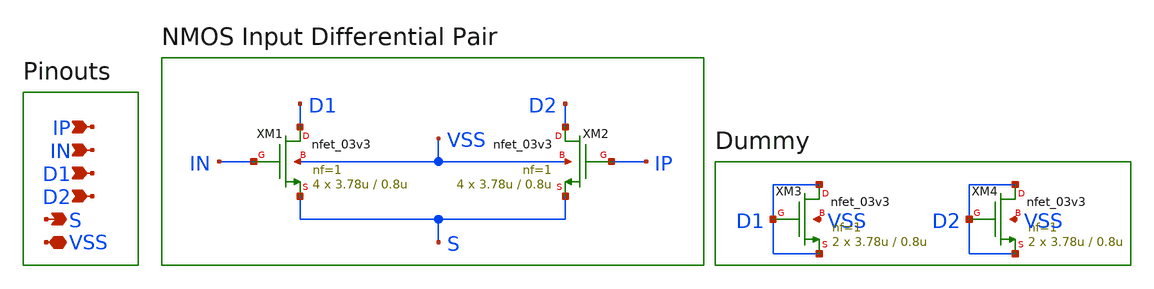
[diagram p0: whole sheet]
** sch_path: designs/libs/core_ota/input_pair/input_pair.sch
**.subckt input_pair VSS S D1 D2 IN IP
*.iopin VSS
*.opin S
*.ipin D1
*.ipin D2
*.ipin IN
*.ipin IP
XM1 D1 IN S VSS nfet_03v3 L=0.8u W=3.78u nf=1 ad='int((nf+1)/2) * W/nf * 0.18u' as='int((nf+2)/2) * W/nf * 0.18u'
+ pd='2*int((nf+1)/2) * (W/nf + 0.18u)' ps='2*int((nf+2)/2) * (W/nf + 0.18u)' nrd='0.18u / W' nrs='0.18u / W'
+ sa=0 sb=0 sd=0 m=4
XM2 D2 IP S VSS nfet_03v3 L=0.8u W=3.78u nf=1 ad='int((nf+1)/2) * W/nf * 0.18u' as='int((nf+2)/2) * W/nf * 0.18u'
+ pd='2*int((nf+1)/2) * (W/nf + 0.18u)' ps='2*int((nf+2)/2) * (W/nf + 0.18u)' nrd='0.18u / W' nrs='0.18u / W'
+ sa=0 sb=0 sd=0 m=4
XM3 D1 D1 D1 VSS nfet_03v3 L=0.8u W=3.78u nf=1 ad='int((nf+1)/2) * W/nf * 0.18u' as='int((nf+2)/2) * W/nf * 0.18u'
+ pd='2*int((nf+1)/2) * (W/nf + 0.18u)' ps='2*int((nf+2)/2) * (W/nf + 0.18u)' nrd='0.18u / W' nrs='0.18u / W'
+ sa=0 sb=0 sd=0 m=2
XM4 D2 D2 D2 VSS nfet_03v3 L=0.8u W=3.78u nf=1 ad='int((nf+1)/2) * W/nf * 0.18u' as='int((nf+2)/2) * W/nf * 0.18u'
+ pd='2*int((nf+1)/2) * (W/nf + 0.18u)' ps='2*int((nf+2)/2) * (W/nf + 0.18u)' nrd='0.18u / W' nrs='0.18u / W'
+ sa=0 sb=0 sd=0 m=2
**.ends
.end
